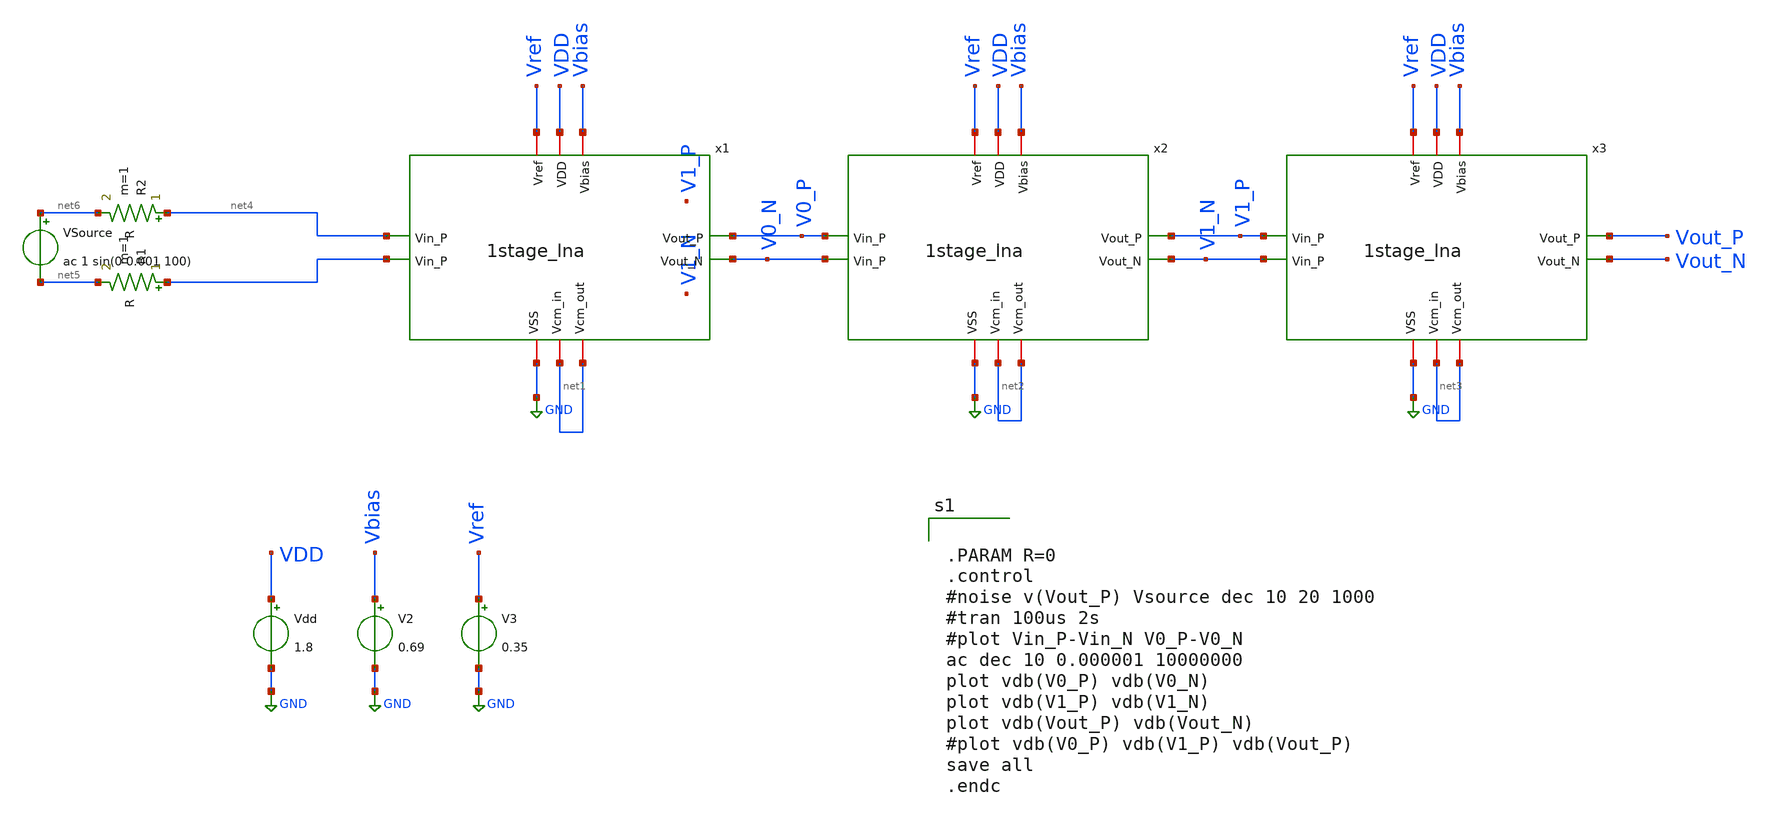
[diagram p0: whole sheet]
** sch_path: opamp_lna/3stage_tb_v2.sch
**.subckt 3stage_tb_v2
Vdd VDD GND 1.8
V2 Vbias GND 0.69
V3 Vref GND 0.35
VSource net6 net5 ac 1 sin(0 0.001 100)
x1 Vref VDD Vbias net4 V0_N V0_N net1 net1 GND 1stage_lna
x2 Vref VDD Vbias V0_N V1_N V1_N net2 net2 GND 1stage_lna
x3 Vref VDD Vbias V1_N Vout_P Vout_N net3 net3 GND 1stage_lna
R1 net4 net5 R m=1
R2 net4 net6 R m=1
**** begin user architecture code

** opencircuitdesign pdks install
.lib $::SKYWATER_MODELS/sky130.lib.spice tt




.PARAM R=0
.control
#noise v(Vout_P) Vsource dec 10 20 1000
#tran 100us 2s
#plot Vin_P-Vin_N V0_P-V0_N
ac dec 10 0.000001 10000000
plot vdb(V0_P) vdb(V0_N)
plot vdb(V1_P) vdb(V1_N)
plot vdb(Vout_P) vdb(Vout_N)
#plot vdb(V0_P) vdb(V1_P) vdb(Vout_P)
save all
.endc

**** end user architecture code
**.ends

* expanding   symbol:  /home/lcg3895/CE393/1stage_lna.sym # of pins=10
** sym_path: opamp_lna/1stage_lna.sym
** sch_path: opamp_lna/1stage_lna.sch
.subckt 1stage_lna Vref VDD Vbias Vin_P Vout_P Vout_N Vcm_out Vcm_in VSS
*.iopin VDD
*.iopin Vbias
*.iopin Vref
*.iopin VSS
*.iopin Vcm_in
*.iopin Vcm_out
*.ipin Vin_P
*.ipin Vin_P
*.opin Vout_N
*.opin Vout_P
x1 VDD Vcm_in net1 net2 Vout_P Vout_N VSS Vcm_out Vbias Vref low_noise_amp
x2 net1 Vout_P pseudoresistor
XC1 net1 Vout_P sky130_fd_pr__cap_mim_m3_1 W=1 L=1 MF=1 m=1
x3 net2 Vout_N pseudoresistor
XC2 net2 Vout_N sky130_fd_pr__cap_mim_m3_1 W=1 L=1 MF=1 m=1
XC8 Vin_P net1 sky130_fd_pr__cap_mim_m3_1 W=150 L=150 MF=1 m=1
XC3 Vin_P net2 sky130_fd_pr__cap_mim_m3_1 W=150 L=150 MF=1 m=1
.ends


* expanding   symbol:  opamp_lna/low_noise_amp.sym # of pins=10
** sym_path: opamp_lna/low_noise_amp.sym
** sch_path: opamp_lna/low_noise_amp.sch
.subckt low_noise_amp VDD Vcm_in INN INP V1P V1N VSS Vcm_out Vbias Vref
*.iopin VDD
*.iopin VSS
*.iopin Vbias
*.ipin INP
*.ipin INN
*.iopin Vref
*.iopin Vcm_in
*.iopin Vcm_out
*.opin V1N
*.opin V1P
XM3 CMFB Vref A0 VDD sky130_fd_pr__pfet_01v8 L=0.8 W=8 nf=1 ad='int((nf+1)/2) * W/nf * 0.29' as='int((nf+2)/2) * W/nf * 0.29'
+ pd='2*int((nf+1)/2) * (W/nf + 0.29)' ps='2*int((nf+2)/2) * (W/nf + 0.29)' nrd='0.29 / W' nrs='0.29 / W'
+ sa=0 sb=0 sd=0 mult=1 m=1
XM11 A0 Vbias VDD VDD sky130_fd_pr__pfet_01v8 L=0.8 W=4 nf=1 ad='int((nf+1)/2) * W/nf * 0.29' as='int((nf+2)/2) * W/nf * 0.29'
+ pd='2*int((nf+1)/2) * (W/nf + 0.29)' ps='2*int((nf+2)/2) * (W/nf + 0.29)' nrd='0.29 / W' nrs='0.29 / W'
+ sa=0 sb=0 sd=0 mult=1 m=1
XM7 V1N INP B0 VDD sky130_fd_pr__pfet_01v8 L=2 W=18 nf=1 ad='int((nf+1)/2) * W/nf * 0.29' as='int((nf+2)/2) * W/nf * 0.29'
+ pd='2*int((nf+1)/2) * (W/nf + 0.29)' ps='2*int((nf+2)/2) * (W/nf + 0.29)' nrd='0.29 / W' nrs='0.29 / W'
+ sa=0 sb=0 sd=0 mult=1 m=1
XM8 V1P INN B0 VDD sky130_fd_pr__pfet_01v8 L=2 W=18 nf=1 ad='int((nf+1)/2) * W/nf * 0.29' as='int((nf+2)/2) * W/nf * 0.29'
+ pd='2*int((nf+1)/2) * (W/nf + 0.29)' ps='2*int((nf+2)/2) * (W/nf + 0.29)' nrd='0.29 / W' nrs='0.29 / W'
+ sa=0 sb=0 sd=0 mult=1 m=1
XM9 V1N INP B1 VSS sky130_fd_pr__nfet_01v8 L=1 W=12 nf=1 ad='int((nf+1)/2) * W/nf * 0.29' as='int((nf+2)/2) * W/nf * 0.29'
+ pd='2*int((nf+1)/2) * (W/nf + 0.29)' ps='2*int((nf+2)/2) * (W/nf + 0.29)' nrd='0.29 / W' nrs='0.29 / W'
+ sa=0 sb=0 sd=0 mult=1 m=1
XM12 B0 Vbias VDD VDD sky130_fd_pr__pfet_01v8 L=0.8 W=4 nf=1 ad='int((nf+1)/2) * W/nf * 0.29' as='int((nf+2)/2) * W/nf * 0.29'
+ pd='2*int((nf+1)/2) * (W/nf + 0.29)' ps='2*int((nf+2)/2) * (W/nf + 0.29)' nrd='0.29 / W' nrs='0.29 / W'
+ sa=0 sb=0 sd=0 mult=1 m=1
XM13 B1 CMFB VSS VSS sky130_fd_pr__nfet_01v8 L=0.8 W=2 nf=1 ad='int((nf+1)/2) * W/nf * 0.29' as='int((nf+2)/2) * W/nf * 0.29'
+ pd='2*int((nf+1)/2) * (W/nf + 0.29)' ps='2*int((nf+2)/2) * (W/nf + 0.29)' nrd='0.29 / W' nrs='0.29 / W'
+ sa=0 sb=0 sd=0 mult=1 m=1
XM15 Vcm_out Vcm_out net1 Vcm_out sky130_fd_pr__pfet_01v8 L=0.6 W=1 nf=1 ad='int((nf+1)/2) * W/nf * 0.29'
+ as='int((nf+2)/2) * W/nf * 0.29' pd='2*int((nf+1)/2) * (W/nf + 0.29)' ps='2*int((nf+2)/2) * (W/nf + 0.29)'
+ nrd='0.29 / W' nrs='0.29 / W' sa=0 sb=0 sd=0 mult=5 m=5
XM16 net1 V1P V1P V1P sky130_fd_pr__pfet_01v8 L=0.6 W=1 nf=1 ad='int((nf+1)/2) * W/nf * 0.29' as='int((nf+2)/2) * W/nf * 0.29'
+ pd='2*int((nf+1)/2) * (W/nf + 0.29)' ps='2*int((nf+2)/2) * (W/nf + 0.29)' nrd='0.29 / W' nrs='0.29 / W'
+ sa=0 sb=0 sd=0 mult=5 m=5
XM17 Vcm_out Vcm_out net2 Vcm_out sky130_fd_pr__pfet_01v8 L=0.6 W=1 nf=1 ad='int((nf+1)/2) * W/nf * 0.29'
+ as='int((nf+2)/2) * W/nf * 0.29' pd='2*int((nf+1)/2) * (W/nf + 0.29)' ps='2*int((nf+2)/2) * (W/nf + 0.29)'
+ nrd='0.29 / W' nrs='0.29 / W' sa=0 sb=0 sd=0 mult=5 m=5
XM18 net2 V1N V1N V1N sky130_fd_pr__pfet_01v8 L=0.6 W=1 nf=1 ad='int((nf+1)/2) * W/nf * 0.29' as='int((nf+2)/2) * W/nf * 0.29'
+ pd='2*int((nf+1)/2) * (W/nf + 0.29)' ps='2*int((nf+2)/2) * (W/nf + 0.29)' nrd='0.29 / W' nrs='0.29 / W'
+ sa=0 sb=0 sd=0 mult=5 m=5
XC1 Vcm_out VSS sky130_fd_pr__cap_mim_m3_1 W=1 L=1 MF=1 m=1
XM1 V1P INN B1 VSS sky130_fd_pr__nfet_01v8 L=1 W=12 nf=1 ad='int((nf+1)/2) * W/nf * 0.29' as='int((nf+2)/2) * W/nf * 0.29'
+ pd='2*int((nf+1)/2) * (W/nf + 0.29)' ps='2*int((nf+2)/2) * (W/nf + 0.29)' nrd='0.29 / W' nrs='0.29 / W'
+ sa=0 sb=0 sd=0 mult=1 m=1
XM2 A1 A1 VSS VSS sky130_fd_pr__nfet_01v8 L=0.8 W=6 nf=1 ad='int((nf+1)/2) * W/nf * 0.29' as='int((nf+2)/2) * W/nf * 0.29'
+ pd='2*int((nf+1)/2) * (W/nf + 0.29)' ps='2*int((nf+2)/2) * (W/nf + 0.29)' nrd='0.29 / W' nrs='0.29 / W'
+ sa=0 sb=0 sd=0 mult=1 m=1
XM5 CMFB A1 VSS VSS sky130_fd_pr__nfet_01v8 L=0.8 W=6 nf=1 ad='int((nf+1)/2) * W/nf * 0.29' as='int((nf+2)/2) * W/nf * 0.29'
+ pd='2*int((nf+1)/2) * (W/nf + 0.29)' ps='2*int((nf+2)/2) * (W/nf + 0.29)' nrd='0.29 / W' nrs='0.29 / W'
+ sa=0 sb=0 sd=0 mult=1 m=1
XM6 A1 Vcm_in A0 VDD sky130_fd_pr__pfet_01v8 L=0.8 W=8 nf=1 ad='int((nf+1)/2) * W/nf * 0.29' as='int((nf+2)/2) * W/nf * 0.29'
+ pd='2*int((nf+1)/2) * (W/nf + 0.29)' ps='2*int((nf+2)/2) * (W/nf + 0.29)' nrd='0.29 / W' nrs='0.29 / W'
+ sa=0 sb=0 sd=0 mult=1 m=1
.ends


* expanding   symbol:  pseudoresistor.sym # of pins=2
** sym_path: opamp_lna/pseudoresistor.sym
** sch_path: opamp_lna/pseudoresistor.sch
.subckt pseudoresistor IN OUT
*.iopin IN
*.iopin OUT
XM5 net1 IN IN IN sky130_fd_pr__pfet_01v8 L=0.5 W=1 nf=5 ad='int((nf+1)/2) * W/nf * 0.29' as='int((nf+2)/2) * W/nf * 0.29'
+ pd='2*int((nf+1)/2) * (W/nf + 0.29)' ps='2*int((nf+2)/2) * (W/nf + 0.29)' nrd='0.29 / W' nrs='0.29 / W'
+ sa=0 sb=0 sd=0 mult=1 m=1
XM1 net2 net2 net1 net2 sky130_fd_pr__pfet_01v8 L=0.5 W=1 nf=5 ad='int((nf+1)/2) * W/nf * 0.29' as='int((nf+2)/2) * W/nf * 0.29'
+ pd='2*int((nf+1)/2) * (W/nf + 0.29)' ps='2*int((nf+2)/2) * (W/nf + 0.29)' nrd='0.29 / W' nrs='0.29 / W'
+ sa=0 sb=0 sd=0 mult=1 m=1
XM2 net3 net2 net2 net2 sky130_fd_pr__pfet_01v8 L=0.5 W=1 nf=5 ad='int((nf+1)/2) * W/nf * 0.29' as='int((nf+2)/2) * W/nf * 0.29'
+ pd='2*int((nf+1)/2) * (W/nf + 0.29)' ps='2*int((nf+2)/2) * (W/nf + 0.29)' nrd='0.29 / W' nrs='0.29 / W'
+ sa=0 sb=0 sd=0 mult=1 m=1
XM3 OUT OUT net3 OUT sky130_fd_pr__pfet_01v8 L=0.5 W=1 nf=5 ad='int((nf+1)/2) * W/nf * 0.29' as='int((nf+2)/2) * W/nf * 0.29'
+ pd='2*int((nf+1)/2) * (W/nf + 0.29)' ps='2*int((nf+2)/2) * (W/nf + 0.29)' nrd='0.29 / W' nrs='0.29 / W'
+ sa=0 sb=0 sd=0 mult=1 m=1
.ends

.GLOBAL GND
.end
